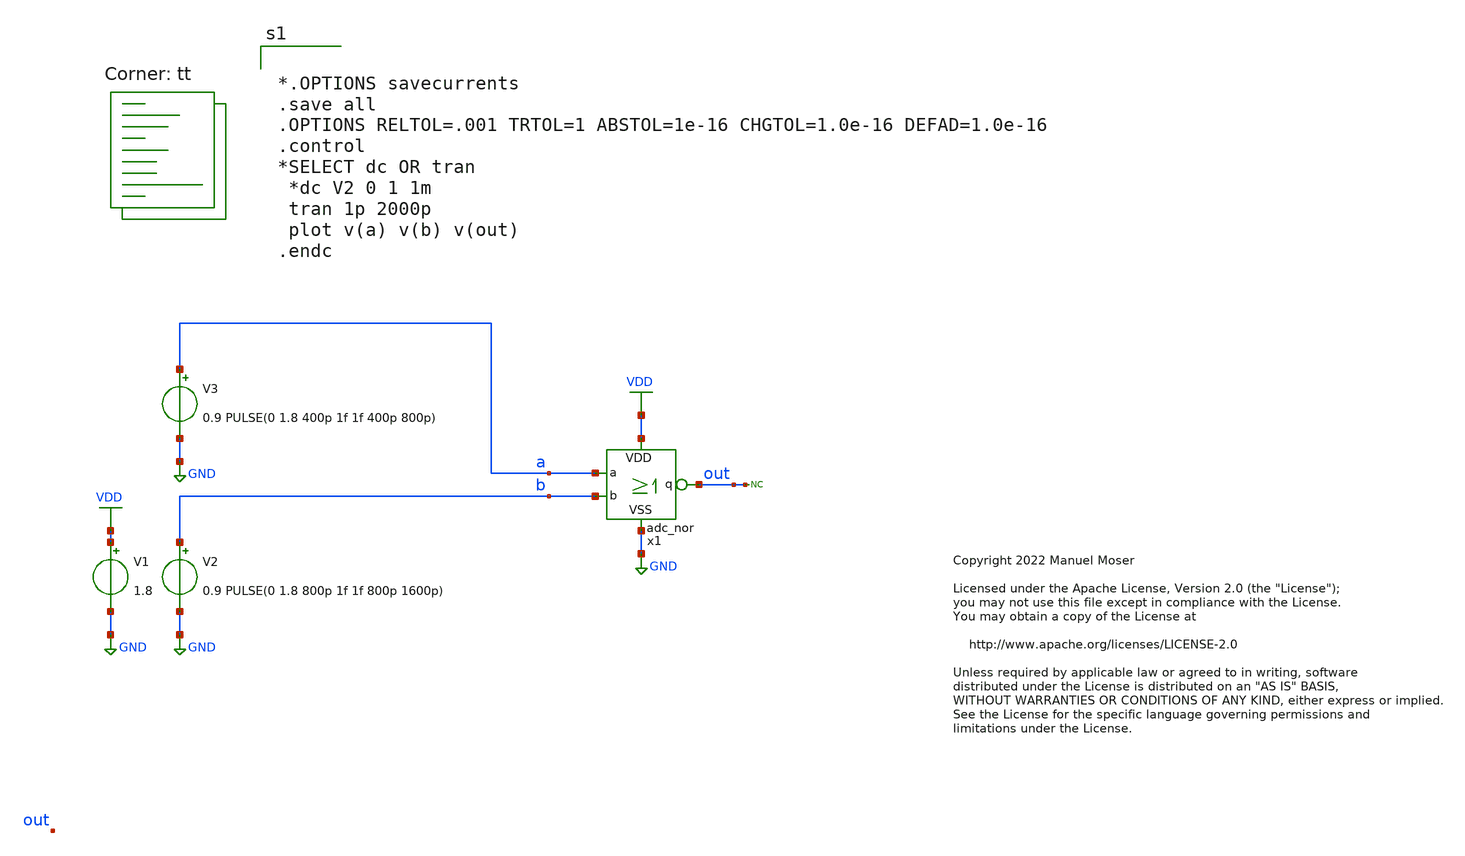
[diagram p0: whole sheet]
** sch_path: xschem/adc_nor_tb.sch
* Copyright 2022 Manuel Moser
* Licensed under the Apache License, Version 2.0 (the "License");
**.subckt adc_nor_tb
V1 VDD GND 1.8
V3 a GND 0.9 PULSE(0 1.8 400p 1f 1f 400p 800p)
V2 b GND 0.9 PULSE(0 1.8 800p 1f 1f 800p 1600p)
* noconn out
x1 b a VDD out GND adc_nor
**** begin user architecture code


*.OPTIONS savecurrents
.save all
.OPTIONS RELTOL=.001 TRTOL=1 ABSTOL=1e-16 CHGTOL=1.0e-16 DEFAD=1.0e-16
.control
*SELECT dc OR tran
 *dc V2 0 1 1m
 tran 1p 2000p
 plot v(a) v(b) v(out)
.endc


.lib $::SKYWATER_MODELS/sky130.lib.spice tt
**** end user architecture code
**.ends

* expanding   symbol:  adc_nor.sym # of pins=5
** sym_path: xschem/adc_nor.sym
** sch_path: xschem/adc_nor.sch
.subckt adc_nor b a VDD q VSS
*.iopin VDD
*.iopin VSS
*.ipin b
*.ipin a
*.opin q
XM5 q b VSS VSS sky130_fd_pr__nfet_01v8 L=0.15 W=0.42 nf=1 ad='int((nf+1)/2) * W/nf * 0.29' as='int((nf+2)/2) * W/nf * 0.29'
+ pd='2*int((nf+1)/2) * (W/nf + 0.29)' ps='2*int((nf+2)/2) * (W/nf + 0.29)' nrd='0.29 / W' nrs='0.29 / W'
+ sa=0 sb=0 sd=0 mult=1 m=1
XM6 q a VSS VSS sky130_fd_pr__nfet_01v8 L=0.15 W=0.42 nf=1 ad='int((nf+1)/2) * W/nf * 0.29' as='int((nf+2)/2) * W/nf * 0.29'
+ pd='2*int((nf+1)/2) * (W/nf + 0.29)' ps='2*int((nf+2)/2) * (W/nf + 0.29)' nrd='0.29 / W' nrs='0.29 / W'
+ sa=0 sb=0 sd=0 mult=1 m=1
XM1 q b net1 VDD sky130_fd_pr__pfet_01v8 L=0.15 W=0.8 nf=1 ad='int((nf+1)/2) * W/nf * 0.29' as='int((nf+2)/2) * W/nf * 0.29'
+ pd='2*int((nf+1)/2) * (W/nf + 0.29)' ps='2*int((nf+2)/2) * (W/nf + 0.29)' nrd='0.29 / W' nrs='0.29 / W'
+ sa=0 sb=0 sd=0 mult=1 m=1
XM2 q a net2 VDD sky130_fd_pr__pfet_01v8 L=0.15 W=0.8 nf=1 ad='int((nf+1)/2) * W/nf * 0.29' as='int((nf+2)/2) * W/nf * 0.29'
+ pd='2*int((nf+1)/2) * (W/nf + 0.29)' ps='2*int((nf+2)/2) * (W/nf + 0.29)' nrd='0.29 / W' nrs='0.29 / W'
+ sa=0 sb=0 sd=0 mult=1 m=1
XM3 net2 b VDD VDD sky130_fd_pr__pfet_01v8 L=0.15 W=0.8 nf=1 ad='int((nf+1)/2) * W/nf * 0.29' as='int((nf+2)/2) * W/nf * 0.29'
+ pd='2*int((nf+1)/2) * (W/nf + 0.29)' ps='2*int((nf+2)/2) * (W/nf + 0.29)' nrd='0.29 / W' nrs='0.29 / W'
+ sa=0 sb=0 sd=0 mult=1 m=1
XM4 net1 a VDD VDD sky130_fd_pr__pfet_01v8 L=0.15 W=0.8 nf=1 ad='int((nf+1)/2) * W/nf * 0.29' as='int((nf+2)/2) * W/nf * 0.29'
+ pd='2*int((nf+1)/2) * (W/nf + 0.29)' ps='2*int((nf+2)/2) * (W/nf + 0.29)' nrd='0.29 / W' nrs='0.29 / W'
+ sa=0 sb=0 sd=0 mult=1 m=1
.ends

.GLOBAL GND
.GLOBAL VDD
.end
